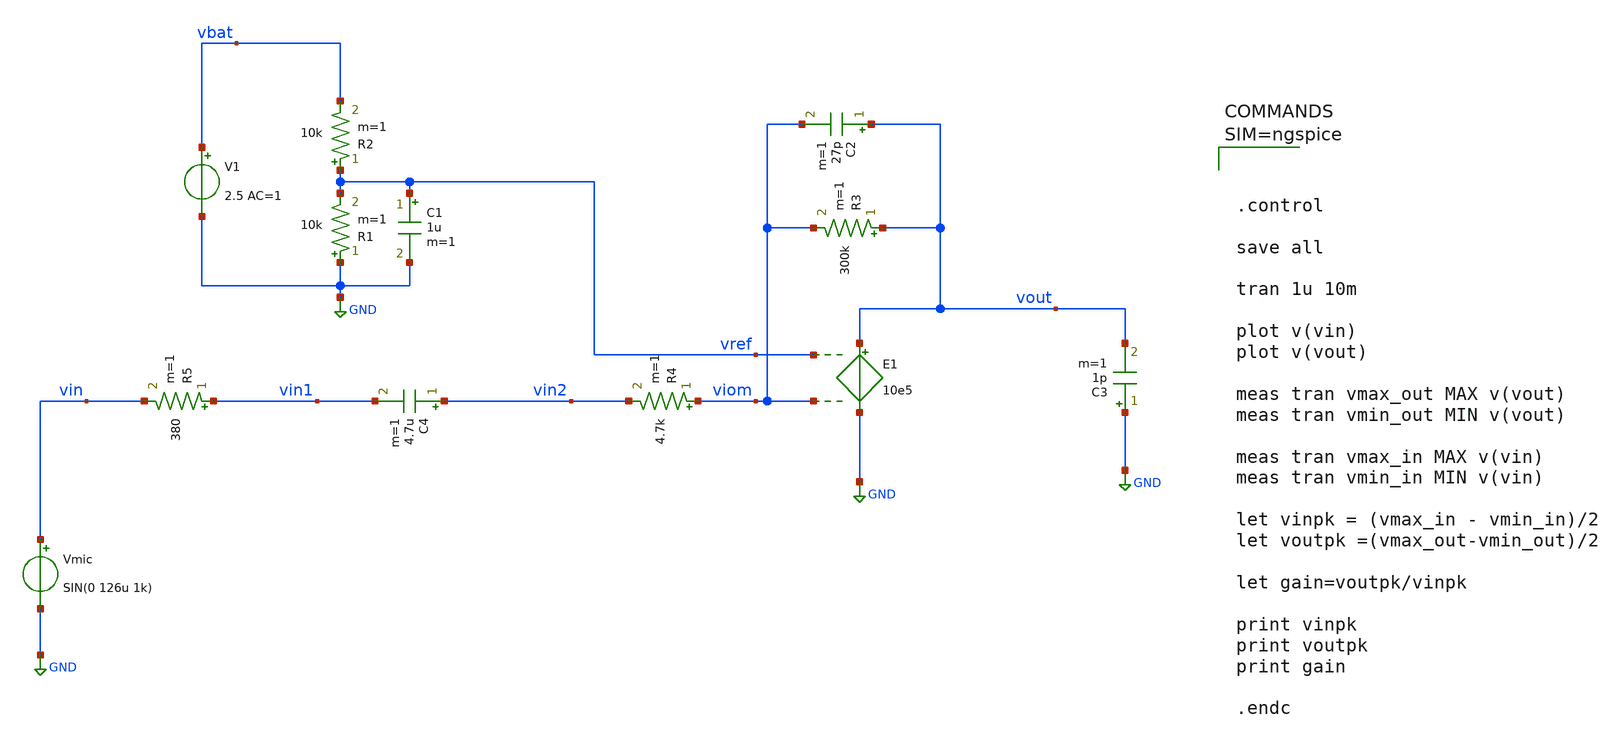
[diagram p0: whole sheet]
** sch_path: xschem/mic_change_final3.sch
**.subckt mic_change_final3
R1 GND vref 10k m=1
R2 vref vbat 10k m=1
C1 vref GND 1u m=1
V1 vbat GND 2.5 AC=1
R3 vout viom 300k m=1
R4 viom vin2 4.7k m=1
R5 vin1 vin 380 m=1
C2 vout viom 27p m=1
E1 vout GND vref viom 10e5
C3 GND vout 1p m=1
C4 vin2 vin1 4.7u m=1
Vmic vin GND SIN(0 126u 1k)
**** begin user architecture code




.control

save all

tran 1u 10m

plot v(vin)
plot v(vout)

meas tran vmax_out MAX v(vout)
meas tran vmin_out MIN v(vout)

meas tran vmax_in MAX v(vin)
meas tran vmin_in MIN v(vin)

let vinpk = (vmax_in - vmin_in)/2
let voutpk =(vmax_out-vmin_out)/2

let gain=voutpk/vinpk

print vinpk
print voutpk
print gain

.endc




**** end user architecture code
**.ends
.GLOBAL GND
.end
